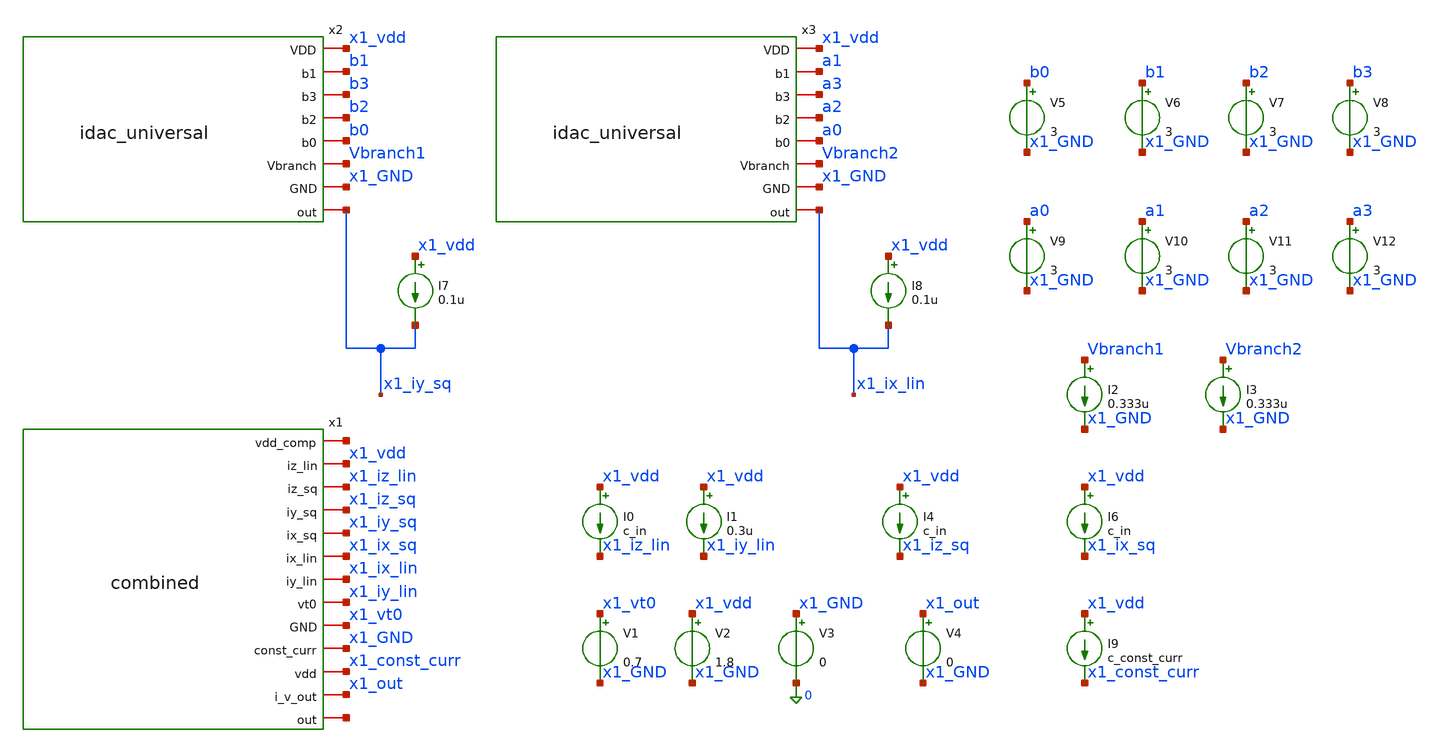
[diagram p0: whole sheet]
** sch_path: xschem/archive/old_blocks/idac_poly.sch
**.subckt idac_poly
x1 net1 x1_vdd x1_iz_lin x1_iz_sq x1_iy_sq x1_ix_sq x1_ix_lin x1_iy_lin x1_vt0 x1_GND x1_const_curr
+ x1_out net2 combined
x2 x1_vdd b1 b3 b2 b0 Vbranch1 x1_GND x1_iy_sq idac_universal
x3 x1_vdd a1 a3 a2 a0 Vbranch2 x1_GND x1_ix_lin idac_universal
I7 x1_vdd x1_iy_sq 0.1u
I8 x1_vdd x1_ix_lin 0.1u
V5 b0 x1_GND 3
V6 b1 x1_GND 3
V7 b2 x1_GND 3
V8 b3 x1_GND 3
V9 a0 x1_GND 3
V10 a1 x1_GND 3
V11 a2 x1_GND 3
V12 a3 x1_GND 3
I2 Vbranch1 x1_GND 0.333u
I0 x1_vdd x1_iz_lin c_in
I1 x1_vdd x1_iy_lin 0.3u
I4 x1_vdd x1_iz_sq c_in
I6 x1_vdd x1_ix_sq c_in
V1 x1_vt0 x1_GND 0.7
V2 x1_vdd x1_GND 1.8
V3 x1_GND 0 0
I9 x1_vdd x1_const_curr c_const_curr
V4 x1_out x1_GND 0
I3 Vbranch2 x1_GND 0.333u
**.ends

* expanding   symbol:  combined.sym # of pins=13
** sym_path: xschem/blocks/combined.sym
** sch_path: xschem/blocks/combined.sch
.subckt combined vdd_comp iz_lin iz_sq iy_sq ix_sq ix_lin iy_lin vt0 GND const_curr vdd i_v_out out
*.iopin vt0
*.iopin ix_sq
*.iopin iy_sq
*.iopin iz_sq
*.iopin vdd_comp
*.iopin ix_lin
*.iopin iy_lin
*.iopin iz_lin
*.iopin out
*.iopin const_curr
*.iopin i_v_out
*.iopin vdd
*.iopin GND
XM18 net1 ix_sq out GND sky130_fd_pr__nfet_01v8 L=4 W=1.2 nf=1 ad='int((nf+1)/2) * W/nf * 0.29' as='int((nf+2)/2) * W/nf * 0.29'
+ pd='2*int((nf+1)/2) * (W/nf + 0.29)' ps='2*int((nf+2)/2) * (W/nf + 0.29)' nrd='0.29 / W' nrs='0.29 / W'
+ sa=0 sb=0 sd=0 mult=1 m=1
XM1 ix_sq vt0 net1 GND sky130_fd_pr__nfet_01v8 L=4 W=8 nf=1 ad='int((nf+1)/2) * W/nf * 0.29' as='int((nf+2)/2) * W/nf * 0.29'
+ pd='2*int((nf+1)/2) * (W/nf + 0.29)' ps='2*int((nf+2)/2) * (W/nf + 0.29)' nrd='0.29 / W' nrs='0.29 / W'
+ sa=0 sb=0 sd=0 mult=20 m=20
XM2 net2 iz_sq out GND sky130_fd_pr__nfet_01v8 L=4 W=1.2 nf=1 ad='int((nf+1)/2) * W/nf * 0.29' as='int((nf+2)/2) * W/nf * 0.29'
+ pd='2*int((nf+1)/2) * (W/nf + 0.29)' ps='2*int((nf+2)/2) * (W/nf + 0.29)' nrd='0.29 / W' nrs='0.29 / W'
+ sa=0 sb=0 sd=0 mult=1 m=1
XM3 iz_sq iy_sq net2 GND sky130_fd_pr__nfet_01v8 L=4 W=8 nf=1 ad='int((nf+1)/2) * W/nf * 0.29' as='int((nf+2)/2) * W/nf * 0.29'
+ pd='2*int((nf+1)/2) * (W/nf + 0.29)' ps='2*int((nf+2)/2) * (W/nf + 0.29)' nrd='0.29 / W' nrs='0.29 / W'
+ sa=0 sb=0 sd=0 mult=20 m=20
XM4 iy_sq iy_sq net1 GND sky130_fd_pr__nfet_01v8 L=4 W=8 nf=1 ad='int((nf+1)/2) * W/nf * 0.29' as='int((nf+2)/2) * W/nf * 0.29'
+ pd='2*int((nf+1)/2) * (W/nf + 0.29)' ps='2*int((nf+2)/2) * (W/nf + 0.29)' nrd='0.29 / W' nrs='0.29 / W'
+ sa=0 sb=0 sd=0 mult=20 m=20
XM5 sq_out vt0 net2 GND sky130_fd_pr__nfet_01v8 L=4 W=8 nf=1 ad='int((nf+1)/2) * W/nf * 0.29' as='int((nf+2)/2) * W/nf * 0.29'
+ pd='2*int((nf+1)/2) * (W/nf + 0.29)' ps='2*int((nf+2)/2) * (W/nf + 0.29)' nrd='0.29 / W' nrs='0.29 / W'
+ sa=0 sb=0 sd=0 mult=20 m=20
XM26 sq_out sq_out vdd_comp vdd sky130_fd_pr__pfet_01v8 L=4 W=8 nf=1 ad='int((1 + 1)/2) * 8 / 1 * 0.29'
+ as='int((1 + 2)/2) * 8 / 1 * 0.29' pd='2*int((1 + 1)/2) * (8 / 1 + 0.29)' ps='2*int((1 + 2)/2) * (8 / 1 + 0.29)'
+ nrd='0.29 / 8 ' nrs='0.29 / 8 ' sa=0 sb=0 sd=0 mult=20 m=20
XM6 net3 ix_lin out GND sky130_fd_pr__nfet_01v8 L=4 W=1.2 nf=1 ad='int((nf+1)/2) * W/nf * 0.29' as='int((nf+2)/2) * W/nf * 0.29'
+ pd='2*int((nf+1)/2) * (W/nf + 0.29)' ps='2*int((nf+2)/2) * (W/nf + 0.29)' nrd='0.29 / W' nrs='0.29 / W'
+ sa=0 sb=0 sd=0 mult=1 m=1
XM7 ix_lin vt0 net3 GND sky130_fd_pr__nfet_01v8 L=4 W=8 nf=1 ad='int((nf+1)/2) * W/nf * 0.29' as='int((nf+2)/2) * W/nf * 0.29'
+ pd='2*int((nf+1)/2) * (W/nf + 0.29)' ps='2*int((nf+2)/2) * (W/nf + 0.29)' nrd='0.29 / W' nrs='0.29 / W'
+ sa=0 sb=0 sd=0 mult=10 m=10
XM8 net4 iz_lin out GND sky130_fd_pr__nfet_01v8 L=4 W=1.2 nf=1 ad='int((nf+1)/2) * W/nf * 0.29' as='int((nf+2)/2) * W/nf * 0.29'
+ pd='2*int((nf+1)/2) * (W/nf + 0.29)' ps='2*int((nf+2)/2) * (W/nf + 0.29)' nrd='0.29 / W' nrs='0.29 / W'
+ sa=0 sb=0 sd=0 mult=1 m=1
XM9 iz_lin iy_lin net4 GND sky130_fd_pr__nfet_01v8 L=4 W=8 nf=1 ad='int((nf+1)/2) * W/nf * 0.29' as='int((nf+2)/2) * W/nf * 0.29'
+ pd='2*int((nf+1)/2) * (W/nf + 0.29)' ps='2*int((nf+2)/2) * (W/nf + 0.29)' nrd='0.29 / W' nrs='0.29 / W'
+ sa=0 sb=0 sd=0 mult=10 m=10
XM10 iy_lin iy_lin net3 GND sky130_fd_pr__nfet_01v8 L=4 W=8 nf=1 ad='int((nf+1)/2) * W/nf * 0.29' as='int((nf+2)/2) * W/nf * 0.29'
+ pd='2*int((nf+1)/2) * (W/nf + 0.29)' ps='2*int((nf+2)/2) * (W/nf + 0.29)' nrd='0.29 / W' nrs='0.29 / W'
+ sa=0 sb=0 sd=0 mult=10 m=10
XM11 lin_out vt0 net4 GND sky130_fd_pr__nfet_01v8 L=4 W=8 nf=1 ad='int((nf+1)/2) * W/nf * 0.29' as='int((nf+2)/2) * W/nf * 0.29'
+ pd='2*int((nf+1)/2) * (W/nf + 0.29)' ps='2*int((nf+2)/2) * (W/nf + 0.29)' nrd='0.29 / W' nrs='0.29 / W'
+ sa=0 sb=0 sd=0 mult=10 m=10
XM12 lin_out lin_out vdd_comp vdd sky130_fd_pr__pfet_01v8 L=4 W=8 nf=1 ad='int((1 + 1)/2) * 8 / 1 * 0.29'
+ as='int((1 + 2)/2) * 8 / 1 * 0.29' pd='2*int((1 + 1)/2) * (8 / 1 + 0.29)' ps='2*int((1 + 2)/2) * (8 / 1 + 0.29)'
+ nrd='0.29 / 8 ' nrs='0.29 / 8 ' sa=0 sb=0 sd=0 mult=20 m=20
XM13 const_curr sq_out vdd vdd sky130_fd_pr__pfet_01v8 L=4 W=8 nf=1 ad='int((1 + 1)/2) * 8 / 1 * 0.29'
+ as='int((1 + 2)/2) * 8 / 1 * 0.29' pd='2*int((1 + 1)/2) * (8 / 1 + 0.29)' ps='2*int((1 + 2)/2) * (8 / 1 + 0.29)'
+ nrd='0.29 / 8 ' nrs='0.29 / 8 ' sa=0 sb=0 sd=0 mult=20 m=20
XM14 const_curr lin_out vdd vdd sky130_fd_pr__pfet_01v8 L=4 W=8 nf=1 ad='int((1 + 1)/2) * 8 / 1 * 0.29'
+ as='int((1 + 2)/2) * 8 / 1 * 0.29' pd='2*int((1 + 1)/2) * (8 / 1 + 0.29)' ps='2*int((1 + 2)/2) * (8 / 1 + 0.29)'
+ nrd='0.29 / 8 ' nrs='0.29 / 8 ' sa=0 sb=0 sd=0 mult=20 m=20
XM15 const_curr const_curr GND GND sky130_fd_pr__nfet_01v8 L=4 W=8 nf=1 ad='int((nf+1)/2) * W/nf * 0.29'
+ as='int((nf+2)/2) * W/nf * 0.29' pd='2*int((nf+1)/2) * (W/nf + 0.29)' ps='2*int((nf+2)/2) * (W/nf + 0.29)'
+ nrd='0.29 / W' nrs='0.29 / W' sa=0 sb=0 sd=0 mult=20 m=20
XM16 net5 const_curr GND GND sky130_fd_pr__nfet_01v8 L=2 W=8 nf=1 ad='int((nf+1)/2) * W/nf * 0.29' as='int((nf+2)/2) * W/nf * 0.29'
+ pd='2*int((nf+1)/2) * (W/nf + 0.29)' ps='2*int((nf+2)/2) * (W/nf + 0.29)' nrd='0.29 / W' nrs='0.29 / W'
+ sa=0 sb=0 sd=0 mult=20 m=20
XM17 net5 net5 vdd vdd sky130_fd_pr__pfet_01v8 L=2 W=4 nf=1 ad='int((1 + 1)/2) * 4 / 1 * 0.29' as='int((1 + 2)/2) * 4 / 1 * 0.29'
+ pd='2*int((1 + 1)/2) * (4 / 1 + 0.29)' ps='2*int((1 + 2)/2) * (4 / 1 + 0.29)' nrd='0.29 / 4 ' nrs='0.29 / 4 '
+ sa=0 sb=0 sd=0 mult=1 m=1
XM19 net6 net5 vdd vdd sky130_fd_pr__pfet_01v8 L=2 W=4 nf=1 ad='int((1 + 1)/2) * 4 / 1 * 0.29' as='int((1 + 2)/2) * 4 / 1 * 0.29'
+ pd='2*int((1 + 1)/2) * (4 / 1 + 0.29)' ps='2*int((1 + 2)/2) * (4 / 1 + 0.29)' nrd='0.29 / 4 ' nrs='0.29 / 4 '
+ sa=0 sb=0 sd=0 mult=10 m=10
XM20 net6 net6 GND GND sky130_fd_pr__nfet_01v8 L=2 W=8 nf=1 ad='int((nf+1)/2) * W/nf * 0.29' as='int((nf+2)/2) * W/nf * 0.29'
+ pd='2*int((nf+1)/2) * (W/nf + 0.29)' ps='2*int((nf+2)/2) * (W/nf + 0.29)' nrd='0.29 / W' nrs='0.29 / W'
+ sa=0 sb=0 sd=0 mult=1 m=1
XM21 i_v_out net6 GND GND sky130_fd_pr__nfet_01v8 L=2 W=8 nf=1 ad='int((nf+1)/2) * W/nf * 0.29' as='int((nf+2)/2) * W/nf * 0.29'
+ pd='2*int((nf+1)/2) * (W/nf + 0.29)' ps='2*int((nf+2)/2) * (W/nf + 0.29)' nrd='0.29 / W' nrs='0.29 / W'
+ sa=0 sb=0 sd=0 mult=1 m=1
.ends


* expanding   symbol:  idac_universal.sym # of pins=8
** sym_path: xschem/blocks/idac_universal.sym
** sch_path: xschem/blocks/idac_universal.sch
.subckt idac_universal VDD b1 b3 b2 b0 Vbranch GND out
*.iopin out
*.iopin GND
*.iopin VDD
*.iopin b3
*.iopin b2
*.iopin b1
*.iopin b0
*.iopin Vbranch
XM27 net1 Vbranch VDD VDD sky130_fd_pr__pfet_01v8 L=7 W=3 nf=1 ad='int((1 + 1)/2) * 3 / 1 * 0.29' as='int((1 + 2)/2) * 3 / 1 * 0.29'
+ pd='2*int((1 + 1)/2) * (3 / 1 + 0.29)' ps='2*int((1 + 2)/2) * (3 / 1 + 0.29)' nrd='0.29 / 3 ' nrs='0.29 / 3 '
+ sa=0 sb=0 sd=0 mult=8 m=8
XM1 net5 b3 net1 VDD sky130_fd_pr__pfet_01v8 L=0.15 W=3 nf=1 ad='int((1 + 1)/2) * 3 / 1 * 0.29' as='int((1 + 2)/2) * 3 / 1 * 0.29'
+ pd='2*int((1 + 1)/2) * (3 / 1 + 0.29)' ps='2*int((1 + 2)/2) * (3 / 1 + 0.29)' nrd='0.29 / 3 ' nrs='0.29 / 3 '
+ sa=0 sb=0 sd=0 mult=1 m=1
XM2 net4 Vbranch VDD VDD sky130_fd_pr__pfet_01v8 L=7 W=3 nf=1 ad='int((1 + 1)/2) * 3 / 1 * 0.29' as='int((1 + 2)/2) * 3 / 1 * 0.29'
+ pd='2*int((1 + 1)/2) * (3 / 1 + 0.29)' ps='2*int((1 + 2)/2) * (3 / 1 + 0.29)' nrd='0.29 / 3 ' nrs='0.29 / 3 '
+ sa=0 sb=0 sd=0 mult=4 m=4
XM3 net5 b2 net4 VDD sky130_fd_pr__pfet_01v8 L=0.15 W=3 nf=1 ad='int((1 + 1)/2) * 3 / 1 * 0.29' as='int((1 + 2)/2) * 3 / 1 * 0.29'
+ pd='2*int((1 + 1)/2) * (3 / 1 + 0.29)' ps='2*int((1 + 2)/2) * (3 / 1 + 0.29)' nrd='0.29 / 3 ' nrs='0.29 / 3 '
+ sa=0 sb=0 sd=0 mult=1 m=1
XM4 net3 Vbranch VDD VDD sky130_fd_pr__pfet_01v8 L=7 W=3 nf=1 ad='int((1 + 1)/2) * 3 / 1 * 0.29' as='int((1 + 2)/2) * 3 / 1 * 0.29'
+ pd='2*int((1 + 1)/2) * (3 / 1 + 0.29)' ps='2*int((1 + 2)/2) * (3 / 1 + 0.29)' nrd='0.29 / 3 ' nrs='0.29 / 3 '
+ sa=0 sb=0 sd=0 mult=2 m=2
XM5 net5 b1 net3 VDD sky130_fd_pr__pfet_01v8 L=0.15 W=3 nf=1 ad='int((1 + 1)/2) * 3 / 1 * 0.29' as='int((1 + 2)/2) * 3 / 1 * 0.29'
+ pd='2*int((1 + 1)/2) * (3 / 1 + 0.29)' ps='2*int((1 + 2)/2) * (3 / 1 + 0.29)' nrd='0.29 / 3 ' nrs='0.29 / 3 '
+ sa=0 sb=0 sd=0 mult=1 m=1
XM6 net2 Vbranch VDD VDD sky130_fd_pr__pfet_01v8 L=7 W=3 nf=1 ad='int((1 + 1)/2) * 3 / 1 * 0.29' as='int((1 + 2)/2) * 3 / 1 * 0.29'
+ pd='2*int((1 + 1)/2) * (3 / 1 + 0.29)' ps='2*int((1 + 2)/2) * (3 / 1 + 0.29)' nrd='0.29 / 3 ' nrs='0.29 / 3 '
+ sa=0 sb=0 sd=0 mult=1 m=1
XM7 net5 b0 net2 VDD sky130_fd_pr__pfet_01v8 L=0.15 W=3 nf=1 ad='int((1 + 1)/2) * 3 / 1 * 0.29' as='int((1 + 2)/2) * 3 / 1 * 0.29'
+ pd='2*int((1 + 1)/2) * (3 / 1 + 0.29)' ps='2*int((1 + 2)/2) * (3 / 1 + 0.29)' nrd='0.29 / 3 ' nrs='0.29 / 3 '
+ sa=0 sb=0 sd=0 mult=1 m=1
XM18 net5 net5 GND GND sky130_fd_pr__nfet_01v8 L=7 W=3 nf=1 ad='int((nf+1)/2) * W/nf * 0.29' as='int((nf+2)/2) * W/nf * 0.29'
+ pd='2*int((nf+1)/2) * (W/nf + 0.29)' ps='2*int((nf+2)/2) * (W/nf + 0.29)' nrd='0.29 / W' nrs='0.29 / W'
+ sa=0 sb=0 sd=0 mult=20 m=20
XM8 net6 net5 GND GND sky130_fd_pr__nfet_01v8 L=7 W=3 nf=1 ad='int((nf+1)/2) * W/nf * 0.29' as='int((nf+2)/2) * W/nf * 0.29'
+ pd='2*int((nf+1)/2) * (W/nf + 0.29)' ps='2*int((nf+2)/2) * (W/nf + 0.29)' nrd='0.29 / W' nrs='0.29 / W'
+ sa=0 sb=0 sd=0 mult=2 m=2
XM13 net6 net6 VDD VDD sky130_fd_pr__pfet_01v8 L=14 W=6 nf=1 ad='int((1 + 1)/2) * 6 / 1 * 0.29' as='int((1 + 2)/2) * 6 / 1 * 0.29'
+ pd='2*int((1 + 1)/2) * (6 / 1 + 0.29)' ps='2*int((1 + 2)/2) * (6 / 1 + 0.29)' nrd='0.29 / 6 ' nrs='0.29 / 6 '
+ sa=0 sb=0 sd=0 mult=3 m=3
XM9 out net6 VDD VDD sky130_fd_pr__pfet_01v8 L=14 W=6 nf=1 ad='int((1 + 1)/2) * 6 / 1 * 0.29' as='int((1 + 2)/2) * 6 / 1 * 0.29'
+ pd='2*int((1 + 1)/2) * (6 / 1 + 0.29)' ps='2*int((1 + 2)/2) * (6 / 1 + 0.29)' nrd='0.29 / 6 ' nrs='0.29 / 6 '
+ sa=0 sb=0 sd=0 mult=3 m=3
XM10 Vbranch Vbranch VDD VDD sky130_fd_pr__pfet_01v8 L=7 W=3 nf=1 ad='int((1 + 1)/2) * 3 / 1 * 0.29'
+ as='int((1 + 2)/2) * 3 / 1 * 0.29' pd='2*int((1 + 1)/2) * (3 / 1 + 0.29)' ps='2*int((1 + 2)/2) * (3 / 1 + 0.29)'
+ nrd='0.29 / 3 ' nrs='0.29 / 3 ' sa=0 sb=0 sd=0 mult=1 m=1
.ends

.end
